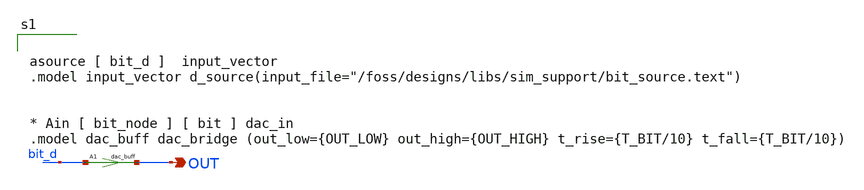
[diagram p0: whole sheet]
** sch_path: designs/libs/sim_support/vbit_file.sch
**.subckt vbit_file OUT
*.opin OUT
A1 [ bit_d ] [ OUT ] dac_buff
**** begin user architecture code


asource [ bit_d ]  input_vector
.model input_vector d_source(input_file="/foss/designs/libs/sim_support/bit_source.text")


* Ain [ bit_node ] [ bit ] dac_in
.model dac_buff dac_bridge (out_low={OUT_LOW} out_high={OUT_HIGH} t_rise={T_BIT/10} t_fall={T_BIT/10})

**** end user architecture code
**.ends
.end
